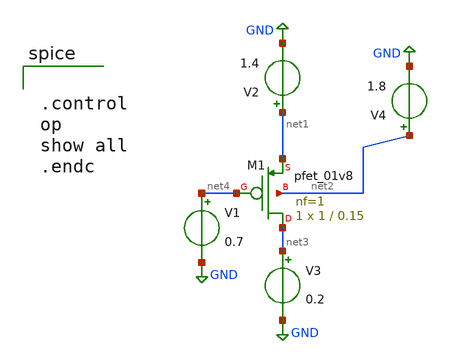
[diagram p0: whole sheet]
** sch_path: pmos.sch
**.subckt pmos
XM1 net3 net4 net1 net2 sky130_fd_pr__pfet_01v8 L=0.15 W=1 nf=1 ad='int((nf+1)/2) * W/nf * 0.29' as='int((nf+2)/2) * W/nf * 0.29'
+ pd='2*int((nf+1)/2) * (W/nf + 0.29)' ps='2*int((nf+2)/2) * (W/nf + 0.29)' nrd='0.29 / W' nrs='0.29 / W'
+ sa=0 sb=0 sd=0 mult=1 m=1
V1 net4 GND 0.7
V2 net1 GND 1.4
V3 net3 GND 0.2
V4 net2 GND 1.8
**** begin user architecture code


.control
op
show all
.endc


*.lib ~/open_pdks/sky130/sky130A/libs.tech/ngspice/sky130.lib.spice tt
.param mc_mm_switch=0
.param mc_pr_switch=0



.include ~/open_pdks/sky130/sky130A/libs.tech/ngspice/corners/tt/nonfet.spice




*model
.include ~/open_pdks/sky130/sky130A/libs.tech/ngspice/all.spice



*mosfet
.include ~/open_pdks/sky130/sky130A/libs.ref/sky130_fd_pr/spice/sky130_fd_pr__pfet_01v8__tt.corner.spice
.inclued ~/open_pdks/sky130/sky130A/libs.ref/sky130_fd_pr/spice/sky130_fd_pr__nfet_01v8__tt.corner.spice



*mismatch parameters
.include ~/open_pdks/sky130/sky130A/libs.ref/sky130_fd_pr/spice/sky130_fd_pr__pfet_01v8__mismatch.corner.spice
.include ~/open_pdks/sky130/sky130A/libs.ref/sky130_fd_pr/spice/sky130_fd_pr__nfet_01v8__mismatch.corner.spice

**** end user architecture code
**.ends
.GLOBAL GND
.end
